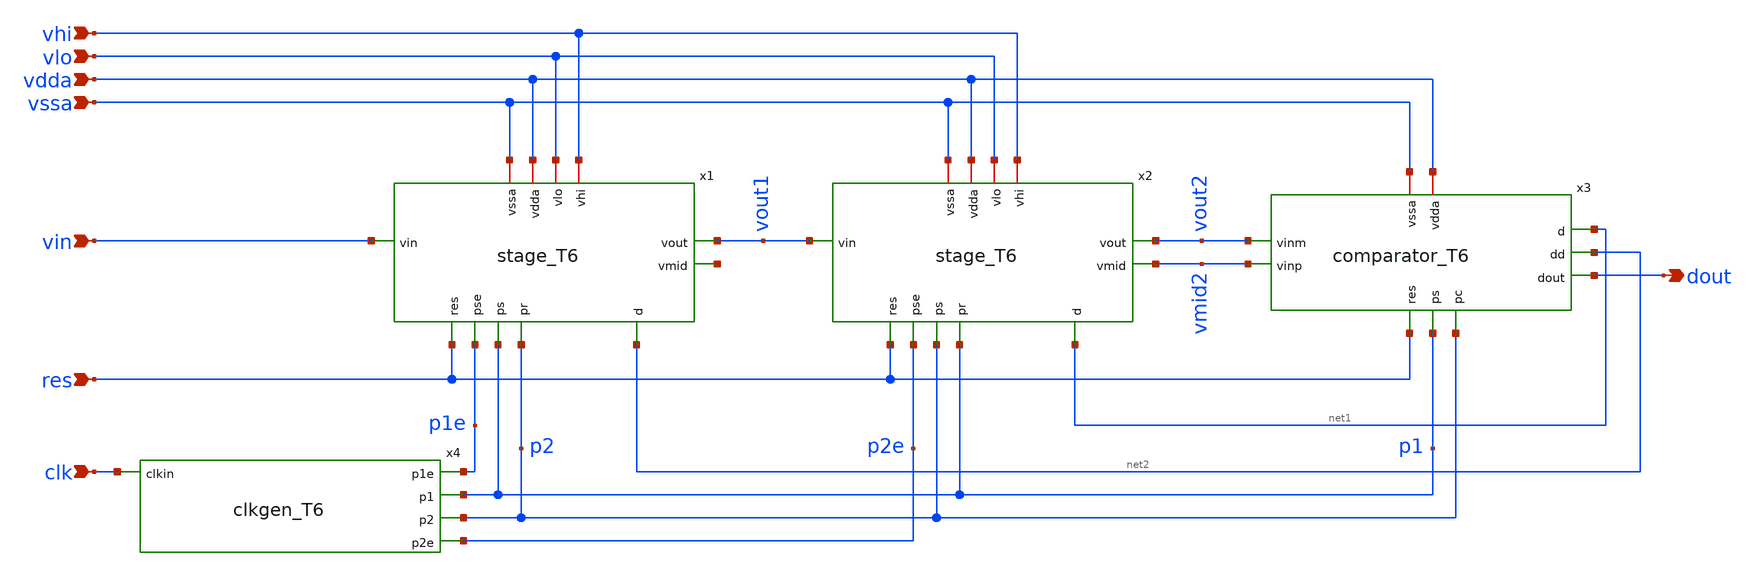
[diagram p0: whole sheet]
** sch_path: 5_Design/4_Layout/Team 6/xschem/Team6.sch
* IHP-GmbH/IHP-Open-PDK/ihp-sg13g2/libs.tech/xschem/sg13g2_stdcells/sg13g2_inv_2.sch:
* Copyright 2023 IHP PDK Authors
* Licensed under the Apache License, Version 2.0 (the "License");
**.subckt Team6 vlo vdda vssa vin vhi res clk dout
*.ipin vlo
*.ipin vdda
*.ipin vssa
*.ipin vin
*.ipin vhi
*.ipin res
*.ipin clk
*.opin dout
x1 res p1e p1 p2 vhi vdda vin vout1 vssa net3 net2 vlo stage_T6
x2 res p2e p2 p1 vhi vdda vout1 vout2 vssa vmid2 net1 vlo stage_T6
x3 vdda p2 net1 vmid2 vssa net2 dout p1 vout2 res comparator_T6
x4 p1e p1 clk p2 p2e clkgen_T6
**.ends

* expanding   symbol:  /foss/designs/ee628/stage_T6.sym # of pins=12
** sym_path: 5_Design/4_Layout/Team 6/xschem/stage_T6.sym
** sch_path: 5_Design/4_Layout/Team 6/xschem/stage_T6.sch
.subckt stage_T6 res pse ps pr vhi vdda vin vout vssa vmid d vlo
*.iopin vhi
*.ipin pr
*.opin vout
*.ipin d
*.ipin vin
*.ipin ps
*.ipin pse
*.ipin res
*.opin vmid
*.iopin vlo
*.iopin vssa
*.iopin vdda
x1 gn pr d VDD VSS sg13g2_and2_1
x2 gp d pr VDD VSS sg13g2_nand2b_1
XC1 vx2 vx1 cap_cmim w=5.77e-6 l=5.77e-6 m=1 mm_ok=1
XM3 vx1 psb vin vdda sg13_lv_pmos w=6.0u l=0.13u ng=3 m=1 mm_ok=1
XM4 vin ps vx1 vssa sg13_lv_nmos w=2.0u l=0.13u ng=1 m=1 mm_ok=1
XM5 vlo gn vx1 vssa sg13_lv_nmos w=0.5u l=0.13u ng=1 m=1 mm_ok=1
XM6 vx1 gp vhi vdda sg13_lv_pmos w=1.5u l=0.13u ng=1 m=1 mm_ok=1
XM7 vmid pse vx2 vssa sg13_lv_nmos w=2u l=0.13u ng=1 m=1 mm_ok=1
XM8 vx2 pr vx4 vssa sg13_lv_nmos w=2u l=0.13u ng=1 m=1 mm_ok=1
XC2 vx3 vx2 cap_cmim w=8.16e-6 l=8.16e-6 m=1 mm_ok=1
XM9 vx3 ps vx4 vssa sg13_lv_nmos w=2u l=0.13u ng=1 m=1 mm_ok=1
XC3 vx4 vout cap_cmim w=8.16e-6 l=8.16e-6 m=1 mm_ok=1
XM10 vx4 res vout vssa sg13_lv_nmos w=2u l=0.13u ng=1 m=1 mm_ok=1
XM11 vout vx3 vdda vdda sg13_lv_pmos w=10u l=1.5u ng=4 m=1 mm_ok=1
XM12 vssa vx3 vout vssa sg13_lv_nmos w=2.5u l=1.5u ng=1 m=1 mm_ok=1
XM1 vmid vmid vdda vdda sg13_lv_pmos w=10u l=1.5u ng=4 m=1 mm_ok=1
XM2 vssa vmid vmid vssa sg13_lv_nmos w=2.5u l=1.5u ng=1 m=1 mm_ok=1
x3 psb ps VDD VSS sg13g2_inv_1
.ends


* expanding   symbol:  /foss/designs/ee628/comparator_T6.sym # of pins=10
** sym_path: 5_Design/4_Layout/Team 6/xschem/comparator_T6.sym
** sch_path: 5_Design/4_Layout/Team 6/xschem/comparator_T6.sch
.subckt comparator_T6 vdda pc d vinp vssa dd dout ps vinm res
*.ipin pc
*.opin d
*.iopin vdda
*.ipin vinp
*.iopin vssa
*.ipin ps
*.ipin vinm
*.ipin res
*.opin dd
*.opin dout
x1 net5 ps VDD VSS sg13g2_inv_1
x2 d din VDD VSS sg13g2_buf_2
XC1 vinm_samp vssa cap_cmim w=5.77e-6 l=5.77e-6 m=1 mm_ok=1
XM1 out1m pc vdda vdda sg13_lv_pmos w=4.0u l=0.13u ng=1 m=1 mm_ok=1
XM2 net3 out1m out1p vssa sg13_lv_nmos w=2.0u l=0.13u ng=1 m=1 mm_ok=1
XM3 out1m out1p vdda vdda sg13_lv_pmos w=4.0u l=0.13u ng=1 m=1 mm_ok=1
XM4 out1p out1m vdda vdda sg13_lv_pmos w=4.0u l=0.13u ng=1 m=1 mm_ok=1
XM5 out1p pc vdda vdda sg13_lv_pmos w=4.0u l=0.13u ng=1 m=1 mm_ok=1
XM6 net1 out1p out1m vssa sg13_lv_nmos w=2.0u l=0.13u ng=1 m=1 mm_ok=1
XM7 net4 pc net3 vssa sg13_lv_nmos w=2.0u l=0.13u ng=1 m=1 mm_ok=1
XM8 net2 pc net1 vssa sg13_lv_nmos w=2.0u l=0.13u ng=1 m=1 mm_ok=1
XM9 vssa vinm_samp net4 vssa sg13_lv_nmos w=2.0u l=1u ng=1 m=1 mm_ok=1
XM10 vssa vinp net2 vssa sg13_lv_nmos w=2.0u l=1u ng=1 m=1 mm_ok=1
XM11 vinm_samp net5 vinm vdda sg13_lv_pmos w=6.0u l=0.13u ng=3 m=1 mm_ok=1
XM12 vinm ps vinm_samp vssa sg13_lv_nmos w=2.0u l=0.13u ng=1 m=1 mm_ok=1
XM13 net6 out1p VDD VDD sg13_lv_pmos w=4.0u l=0.13u ng=1 m=1 mm_ok=1
XM14 net8 net6 din VSS sg13_lv_nmos w=2.0u l=0.13u ng=1 m=1 mm_ok=1
XM15 net6 din VDD VDD sg13_lv_pmos w=4.0u l=0.13u ng=1 m=1 mm_ok=1
XM16 din net6 VDD VDD sg13_lv_pmos w=4.0u l=0.13u ng=1 m=1 mm_ok=1
XM17 din out1m VDD VDD sg13_lv_pmos w=4.0u l=0.13u ng=1 m=1 mm_ok=1
XM18 net7 din net6 VSS sg13_lv_nmos w=2.0u l=0.13u ng=1 m=1 mm_ok=1
XM19 VSS out1m net8 VSS sg13_lv_nmos w=2.0u l=0.13u ng=1 m=1 mm_ok=1
XM20 VSS out1p net7 VSS sg13_lv_nmos w=2.0u l=0.13u ng=1 m=1 mm_ok=1
x4 resb res VDD VSS sg13g2_inv_1
x3 dout dd VDD VSS sg13g2_inv_2
x6 dd net9 ps din resb VDD VSS sg13g2_dfrbp_2
.ends


* expanding   symbol:  /foss/designs/ee628/clkgen_T6.sym # of pins=5
** sym_path: 5_Design/4_Layout/Team 6/xschem/clkgen_T6.sym
** sch_path: 5_Design/4_Layout/Team 6/xschem/clkgen_T6.sch
.subckt clkgen_T6 p1e p1 clkin p2 p2e
*.ipin clkin
*.opin p1e
*.opin p1
*.opin p2
*.opin p2e
x23 clkinb clkin VDD VSS sg13g2_inv_2
x2 clkinbb clkinb VDD VSS sg13g2_inv_2
x3 net7 b1 clkinb VDD VSS sg13g2_nand2_2
x4 net1 clkinbb b2 VDD VSS sg13g2_nand2_2
x14 net3 net2 VDD VSS sg13g2_inv_4
x1 net2 net1 VDD VSS sg13g2_inv_4
x5 net4 net3 VDD VSS sg13g2_inv_4
x6 a1 net4 VDD VSS sg13g2_inv_4
x7 p1e a1 VDD VSS sg13g2_inv_4
x8 b1 p1e VDD VSS sg13g2_inv_4
x9 b2 p2e VDD VSS sg13g2_inv_4
x10 p2e a2 VDD VSS sg13g2_inv_4
x15 a2 net10 VDD VSS sg13g2_inv_4
x16 net10 net9 VDD VSS sg13g2_inv_4
x17 net9 net8 VDD VSS sg13g2_inv_4
x18 net8 net7 VDD VSS sg13g2_inv_4
x11 net5 a1 b1 VDD VSS sg13g2_nand2_2
x19 net11 a2 b2 VDD VSS sg13g2_nand2_2
x12 net6 net5 VDD VSS sg13g2_inv_4
x20 net12 net11 VDD VSS sg13g2_inv_4
x13 p1 net6 VDD VSS sg13g2_inv_8
x21 p2 net12 VDD VSS sg13g2_inv_8
.ends


* expanding   symbol:  sg13g2_stdcells/sg13g2_and2_1.sym # of pins=3
** sym_path: sg13g2_stdcells/sg13g2_and2_1.sym
** sch_path: sg13g2_stdcells/sg13g2_and2_1.sch
.subckt sg13g2_and2_1 X A B VDD VSS
*.ipin A
*.ipin B
*.opin X
*.iopin VDD
*.iopin VSS
XM1 net1 A net2 VSS sg13_lv_nmos w=640.00n l=130.00n ng=1 m=1 mm_ok=1
XM2 net2 B VSS VSS sg13_lv_nmos w=640.00n l=130.00n ng=1 m=1 mm_ok=1
XM3 X net1 VSS VSS sg13_lv_nmos w=740.00n l=130.00n ng=1 m=1 mm_ok=1
XM4 net1 B VDD VDD sg13_lv_pmos w=840.00n l=130.00n ng=1 m=1 mm_ok=1
XM5 net1 A VDD VDD sg13_lv_pmos w=840.00n l=130.00n ng=1 m=1 mm_ok=1
XM6 X net1 VDD VDD sg13_lv_pmos w=1.12u l=130.00n ng=1 m=1 mm_ok=1
.ends


* expanding   symbol:  sg13g2_stdcells/sg13g2_nand2b_1.sym # of pins=3
** sym_path: sg13g2_stdcells/sg13g2_nand2b_1.sym
** sch_path: sg13g2_stdcells/sg13g2_nand2b_1.sch
.subckt sg13g2_nand2b_1 Y A_N B VDD VSS
*.opin Y
*.ipin B
*.ipin A_N
*.iopin VDD
*.iopin VSS
XM1 net1 A_N VSS VSS sg13_lv_nmos w=550.00n l=130.00n ng=1 m=1 mm_ok=1
XM2 Y net1 net2 VSS sg13_lv_nmos w=740.00n l=130.00n ng=1 m=1 mm_ok=1
XM3 net2 B VSS VSS sg13_lv_nmos w=740.00n l=130.00n ng=1 m=1 mm_ok=1
XM4 Y B VDD VDD sg13_lv_pmos w=1.12u l=130.00n ng=1 m=1 mm_ok=1
XM5 net1 A_N VDD VDD sg13_lv_pmos w=840.00n l=130.00n ng=1 m=1 mm_ok=1
XM6 Y net1 VDD VDD sg13_lv_pmos w=1.12u l=130.00n ng=1 m=1 mm_ok=1
.ends


* expanding   symbol:  sg13g2_stdcells/sg13g2_inv_1.sym # of pins=2
** sym_path: sg13g2_stdcells/sg13g2_inv_1.sym
** sch_path: sg13g2_stdcells/sg13g2_inv_1.sch
.subckt sg13g2_inv_1 Y A VDD VSS
*.opin Y
*.ipin A
*.iopin VDD
*.iopin VSS
XM1 Y A VSS VSS sg13_lv_nmos w=740.00n l=130.00n ng=1 m=1 mm_ok=1
XM2 Y A VDD VDD sg13_lv_pmos w=1.12u l=130.00n ng=1 m=1 mm_ok=1
.ends


* expanding   symbol:  sg13g2_stdcells/sg13g2_buf_2.sym # of pins=2
** sym_path: sg13g2_stdcells/sg13g2_buf_2.sym
** sch_path: sg13g2_stdcells/sg13g2_buf_2.sch
.subckt sg13g2_buf_2 X A VDD VSS
*.ipin A
*.opin X
*.iopin VDD
*.iopin VSS
XM1 net1 A VSS VSS sg13_lv_nmos w=640.00n l=130.00n ng=1 m=1 mm_ok=1
XM2 X net1 VSS VSS sg13_lv_nmos w=1.48u l=130.00n ng=2 m=1 mm_ok=1
XM3 net1 A VDD VDD sg13_lv_pmos w=1.000u l=130.00n ng=1 m=1 mm_ok=1
XM4 X net1 VDD VDD sg13_lv_pmos w=2.24u l=130.00n ng=2 m=1 mm_ok=1
.ends


* expanding   symbol:  sg13g2_stdcells/sg13g2_inv_2.sym # of pins=2
** sym_path: sg13g2_stdcells/sg13g2_inv_2.sym
** sch_path: sg13g2_stdcells/sg13g2_inv_2.sch
.subckt sg13g2_inv_2 Y A VDD VSS
*.opin Y
*.ipin A
*.iopin VDD
*.iopin VSS
XM1 Y A VSS VSS sg13_lv_nmos w=1.48u l=130.00n ng=2 m=1 mm_ok=1
XM2 Y A VDD VDD sg13_lv_pmos w=2.24u l=130.00n ng=2 m=1 mm_ok=1
.ends


* expanding   symbol:  sg13g2_stdcells/sg13g2_dfrbp_2.sym # of pins=5
** sym_path: sg13g2_stdcells/sg13g2_dfrbp_2.sym
** sch_path: sg13g2_stdcells/sg13g2_dfrbp_2.sch
.subckt sg13g2_dfrbp_2 Q Q_N CLK D RESET_B VDD VSS
*.ipin D
*.ipin RESET_B
*.ipin CLK
*.opin Q
*.opin Q_N
*.iopin VDD
*.iopin VSS
XM1 Db D net12 VSS sg13_lv_nmos w=420.00n l=130.00n ng=1 m=1 mm_ok=1
XM2 net12 RESET_B VSS VSS sg13_lv_nmos w=420.00n l=130.00n ng=1 m=1 mm_ok=1
XM3 net2 clkneg net11 VSS sg13_lv_nmos w=420.00n l=130.00n ng=1 m=1 mm_ok=1
XM4 net11 net3 VSS VSS sg13_lv_nmos w=420.00n l=130.00n ng=1 m=1 mm_ok=1
XM5 net3 net2 net7 VSS sg13_lv_nmos w=420.00n l=130.00n ng=1 m=1 mm_ok=1
XM6 net7 RESET_B VSS VSS sg13_lv_nmos w=420.00n l=130.00n ng=1 m=1 mm_ok=1
XM7 Q_N net2 VSS VSS sg13_lv_nmos w=1.48u l=130.00n ng=2 m=1 mm_ok=1
XM8 net1 net2 VSS VSS sg13_lv_nmos w=640.00n l=130.00n ng=1 m=1 mm_ok=1
XM9 Q net1 VSS VSS sg13_lv_nmos w=1.48u l=130.00n ng=2 m=1 mm_ok=1
XM10 clkneg CLK VSS VSS sg13_lv_nmos w=740.00n l=130.00n ng=1 m=1 mm_ok=1
XM11 clkpos clkneg VSS VSS sg13_lv_nmos w=740.00n l=130.00n ng=1 m=1 mm_ok=1
XM12 Db clkneg net4 VSS sg13_lv_nmos w=420.00n l=130.00n ng=1 m=1 mm_ok=1
XM13 net4 clkpos net10 VSS sg13_lv_nmos w=420.00n l=130.00n ng=1 m=1 mm_ok=1
XM14 net10 net5 net6 VSS sg13_lv_nmos w=420.00n l=130.00n ng=1 m=1 mm_ok=1
XM15 net6 RESET_B VSS VSS sg13_lv_nmos w=420.00n l=130.00n ng=1 m=1 mm_ok=1
XM16 net5 net4 VSS VSS sg13_lv_nmos w=740.00n l=130.00n ng=1 m=1 mm_ok=1
XM17 net5 clkpos net2 VSS sg13_lv_nmos w=740.00n l=130.00n ng=1 m=1 mm_ok=1
XM18 Db RESET_B VDD VDD sg13_lv_pmos w=420.00n l=130.00n ng=1 m=1 mm_ok=1
XM19 Db D VDD VDD sg13_lv_pmos w=420.00n l=130.00n ng=1 m=1 mm_ok=1
XM20 net9 net3 VDD VDD sg13_lv_pmos w=420.00n l=130.00n ng=1 m=1 mm_ok=1
XM21 net2 clkpos net9 VDD sg13_lv_pmos w=420.00n l=130.00n ng=1 m=1 mm_ok=1
XM22 net3 net2 VDD VDD sg13_lv_pmos w=420.00n l=130.00n ng=1 m=1 mm_ok=1
XM23 net3 RESET_B VDD VDD sg13_lv_pmos w=420.00n l=130.00n ng=1 m=1 mm_ok=1
XM24 Q_N net2 VDD VDD sg13_lv_pmos w=2.24u l=130.00n ng=2 m=1 mm_ok=1
XM25 net1 net2 VDD VDD sg13_lv_pmos w=1.000u l=130.00n ng=1 m=1 mm_ok=1
XM26 Q net1 VDD VDD sg13_lv_pmos w=2.24u l=130.00n ng=2 m=1 mm_ok=1
XM27 clkneg CLK VDD VDD sg13_lv_pmos w=1.12u l=130.00n ng=1 m=1 mm_ok=1
XM28 clkpos clkneg VDD VDD sg13_lv_pmos w=1.12u l=130.00n ng=1 m=1 mm_ok=1
XM29 Db clkpos net4 VDD sg13_lv_pmos w=420.00n l=130.00n ng=1 m=1 mm_ok=1
XM30 net8 net5 VDD VDD sg13_lv_pmos w=420.00n l=130.00n ng=1 m=1 mm_ok=1
XM31 net4 clkneg net8 VDD sg13_lv_pmos w=420.00n l=130.00n ng=1 m=1 mm_ok=1
XM32 net4 RESET_B VDD VDD sg13_lv_pmos w=420.00n l=130.00n ng=1 m=1 mm_ok=1
XM33 net5 net4 VDD VDD sg13_lv_pmos w=1.000u l=130.00n ng=1 m=1 mm_ok=1
XM34 net5 clkneg net2 VDD sg13_lv_pmos w=1.000u l=130.00n ng=1 m=1 mm_ok=1
.ends


* expanding   symbol:  sg13g2_stdcells/sg13g2_nand2_2.sym # of pins=3
** sym_path: sg13g2_stdcells/sg13g2_nand2_2.sym
** sch_path: sg13g2_stdcells/sg13g2_nand2_2.sch
.subckt sg13g2_nand2_2 Y A B VDD VSS
*.iopin VDD
*.iopin VSS
*.opin Y
*.ipin B
*.ipin A
XM1 Y A net1 VSS sg13_lv_nmos w=1.44u l=130.00n ng=2 m=1 mm_ok=1
XM2 net1 B VSS VSS sg13_lv_nmos w=1.44u l=130.00n ng=2 m=1 mm_ok=1
XM3 Y A VDD VDD sg13_lv_pmos w=2.24u l=130.00n ng=2 m=1 mm_ok=1
XM4 Y B VDD VDD sg13_lv_pmos w=2.24u l=130.00n ng=2 m=1 mm_ok=1
.ends


* expanding   symbol:  sg13g2_stdcells/sg13g2_inv_4.sym # of pins=2
** sym_path: sg13g2_stdcells/sg13g2_inv_4.sym
** sch_path: sg13g2_stdcells/sg13g2_inv_4.sch
.subckt sg13g2_inv_4 Y A VDD VSS
*.ipin A
*.opin Y
*.iopin VDD
*.iopin VSS
XM1 Y A VSS VSS sg13_lv_nmos w=2.96u l=130.00n ng=4 m=1 mm_ok=1
XM2 Y A VDD VDD sg13_lv_pmos w=4.48u l=130.00n ng=4 m=1 mm_ok=1
.ends


* expanding   symbol:  sg13g2_stdcells/sg13g2_inv_8.sym # of pins=2
** sym_path: sg13g2_stdcells/sg13g2_inv_8.sym
** sch_path: sg13g2_stdcells/sg13g2_inv_8.sch
.subckt sg13g2_inv_8 Y A VDD VSS
*.opin Y
*.ipin A
*.iopin VDD
*.iopin VSS
XM1 Y A VSS VSS sg13_lv_nmos w=5.92u l=130.00n ng=8 m=1 mm_ok=1
XM2 Y A VDD VDD sg13_lv_pmos w=8.96u l=130.00n ng=8 m=1 mm_ok=1
.ends

.GLOBAL VDD
.GLOBAL VSS
.end
